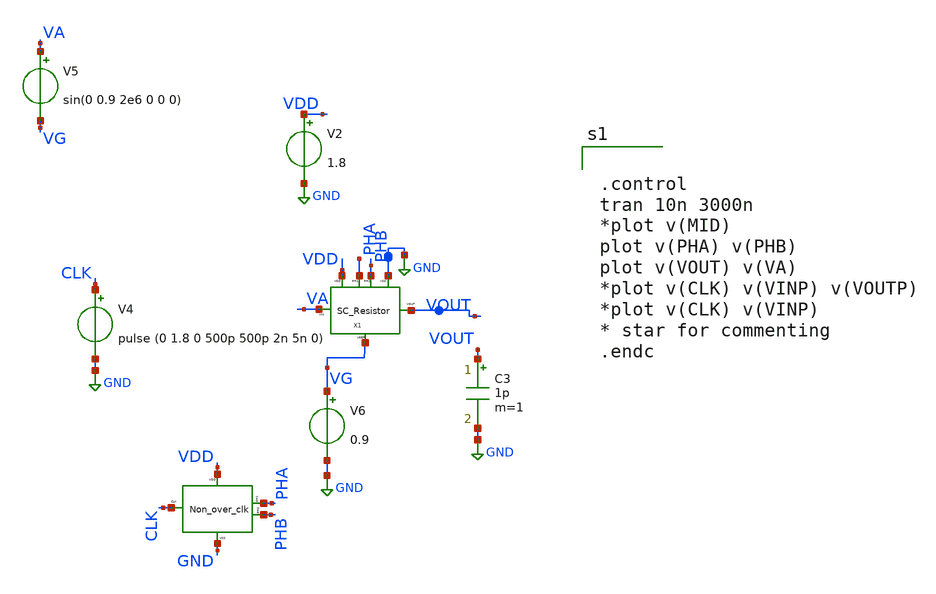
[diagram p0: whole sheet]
** sch_path: xschem/xschem_BGR_Top/Sigma_Delta/SC_Resistor/SC_Resistor_TB.sch
**.subckt SC_Resistor_TB
V2 VDD GND 1.8
V6 VG GND 0.9
X1 VG PHB VOUT VDD GND PHA VA SC_Resistor
V5 VA VG sin(0 0.9 2e6 0 0 0)
X2 PHB VDD GND PHA CLK Non_over_clk
V4 CLK GND pulse (0 1.8 0 500p 500p 2n 5n 0)
C3 VOUT GND 1p m=1
**** begin user architecture code


.control
tran 10n 3000n
*plot v(MID)
plot v(PHA) v(PHB)
plot v(VOUT) v(VA)
*plot v(CLK) v(VINP) v(VOUTP)
*plot v(CLK) v(VINP)
* star for commenting
.endc


** opencircuitdesign pdks install
.lib $::SKYWATER_MODELS/sky130.lib.spice tt


**** end user architecture code
**.ends

* expanding   symbol:  Sigma_Delta/SC_Resistor/SC_Resistor.sym # of pins=7
** sym_path: xschem/xschem_BGR_Top/Sigma_Delta/SC_Resistor/SC_Resistor.sym
** sch_path: xschem/xschem_BGR_Top/Sigma_Delta/SC_Resistor/SC_Resistor.sch
.subckt SC_Resistor VREF PH2 VOUT VDD VSS PH1 VIN
*.iopin VDD
*.iopin PH1
*.iopin VIN
*.iopin VOUT
*.iopin PH2
*.iopin VREF
*.iopin VSS
XTG3 VSS PH1 VDD VIN MID1 TG
XTG4 VSS PH2 VDD MID2 VOUT TG
XM2 MID1 PH2 VREF VSS sky130_fd_pr__nfet_01v8 L=0.15 W=20 nf=2 ad='int((nf+1)/2) * W/nf * 0.29' as='int((nf+2)/2) * W/nf * 0.29'
+ pd='2*int((nf+1)/2) * (W/nf + 0.29)' ps='2*int((nf+2)/2) * (W/nf + 0.29)' nrd='0.29 / W' nrs='0.29 / W'
+ sa=0 sb=0 sd=0 mult=1 m=1
XM1 MID2 PH1 VREF VSS sky130_fd_pr__nfet_01v8 L=0.15 W=20 nf=2 ad='int((nf+1)/2) * W/nf * 0.29' as='int((nf+2)/2) * W/nf * 0.29'
+ pd='2*int((nf+1)/2) * (W/nf + 0.29)' ps='2*int((nf+2)/2) * (W/nf + 0.29)' nrd='0.29 / W' nrs='0.29 / W'
+ sa=0 sb=0 sd=0 mult=1 m=1
XC2 MID2 MID1 sky130_fd_pr__cap_mim_m3_2 W=32 L=32 MF=1 m=1
.ends


* expanding   symbol:  Sigma_Delta/Non_over_clk/Non_over_clk.sym # of pins=5
** sym_path: xschem/xschem_BGR_Top/Sigma_Delta/Non_over_clk/Non_over_clk.sym
** sch_path: xschem/xschem_BGR_Top/Sigma_Delta/Non_over_clk/Non_over_clk.sch
.subckt Non_over_clk PH2 VDD VSS PH1 CLK
*.iopin VDD
*.iopin VSS
*.iopin CLK
*.iopin PH1
*.iopin PH2
X1 VSS VDD CLK net1 Inverter
X2 VSS VDD net9 PH1 Inverter
X3 VSS VDD net8 PH2 Inverter
X4 VSS VDD net3 net2 INV_1x64
X5 VSS VDD net5 net4 INV_1x64
XNOR1 VDD VSS net1 PH2 net3 NOR
XNOR2 VDD VSS CLK PH1 net5 NOR
X8 VSS VDD net6 net8 Inverter
X9 VSS VDD net7 net9 Inverter
X6 VSS VDD net2 net7 INV_1x64
X7 VSS VDD net4 net6 INV_1x64
.ends


* expanding   symbol:  Sigma_Delta/Transmission_Gate/TG.sym # of pins=5
** sym_path: xschem/xschem_BGR_Top/Sigma_Delta/Transmission_Gate/TG.sym
** sch_path: xschem/xschem_BGR_Top/Sigma_Delta/Transmission_Gate/TG.sch
.subckt TG VSS CLK VDD A B
*.iopin VDD
*.iopin VSS
*.iopin A
*.iopin B
*.iopin CLK
XM1 A CLK B VSS sky130_fd_pr__nfet_01v8 L=0.15 W=10 nf=1 ad='int((nf+1)/2) * W/nf * 0.29' as='int((nf+2)/2) * W/nf * 0.29'
+ pd='2*int((nf+1)/2) * (W/nf + 0.29)' ps='2*int((nf+2)/2) * (W/nf + 0.29)' nrd='0.29 / W' nrs='0.29 / W'
+ sa=0 sb=0 sd=0 mult=1 m=1
XM2 B CLKB A VDD sky130_fd_pr__pfet_01v8 L=0.15 W=20 nf=2 ad='int((nf+1)/2) * W/nf * 0.29' as='int((nf+2)/2) * W/nf * 0.29'
+ pd='2*int((nf+1)/2) * (W/nf + 0.29)' ps='2*int((nf+2)/2) * (W/nf + 0.29)' nrd='0.29 / W' nrs='0.29 / W'
+ sa=0 sb=0 sd=0 mult=1 m=1
XM3 CLKB CLK VSS VSS sky130_fd_pr__nfet_01v8 L=0.15 W=10 nf=5 ad='int((nf+1)/2) * W/nf * 0.29' as='int((nf+2)/2) * W/nf * 0.29'
+ pd='2*int((nf+1)/2) * (W/nf + 0.29)' ps='2*int((nf+2)/2) * (W/nf + 0.29)' nrd='0.29 / W' nrs='0.29 / W'
+ sa=0 sb=0 sd=0 mult=1 m=1
XM4 CLKB CLK VDD VDD sky130_fd_pr__pfet_01v8 L=0.15 W=20 nf=10 ad='int((nf+1)/2) * W/nf * 0.29' as='int((nf+2)/2) * W/nf * 0.29'
+ pd='2*int((nf+1)/2) * (W/nf + 0.29)' ps='2*int((nf+2)/2) * (W/nf + 0.29)' nrd='0.29 / W' nrs='0.29 / W'
+ sa=0 sb=0 sd=0 mult=1 m=1
.ends


* expanding   symbol:  Sigma_Delta/Inverter/Inverter.sym # of pins=4
** sym_path: xschem/xschem_BGR_Top/Sigma_Delta/Inverter/Inverter.sym
** sch_path: xschem/xschem_BGR_Top/Sigma_Delta/Inverter/Inverter.sch
.subckt Inverter VSS VDD VIN VOUT
*.ipin VIN
*.iopin VDD
*.iopin VSS
*.opin VOUT
XM1 VOUT VIN VSS VSS sky130_fd_pr__nfet_01v8 L=0.15 W=0.9 nf=1 ad='int((nf+1)/2) * W/nf * 0.29' as='int((nf+2)/2) * W/nf * 0.29'
+ pd='2*int((nf+1)/2) * (W/nf + 0.29)' ps='2*int((nf+2)/2) * (W/nf + 0.29)' nrd='0.29 / W' nrs='0.29 / W'
+ sa=0 sb=0 sd=0 mult=1 m=1
XM2 VOUT VIN VDD VDD sky130_fd_pr__pfet_01v8 L=0.15 W=0.9 nf=2 ad='int((nf+1)/2) * W/nf * 0.29' as='int((nf+2)/2) * W/nf * 0.29'
+ pd='2*int((nf+1)/2) * (W/nf + 0.29)' ps='2*int((nf+2)/2) * (W/nf + 0.29)' nrd='0.29 / W' nrs='0.29 / W'
+ sa=0 sb=0 sd=0 mult=1 m=1
.ends


* expanding   symbol:  Sigma_Delta/INV_1x64/INV_1x64.sym # of pins=4
** sym_path: xschem/xschem_BGR_Top/Sigma_Delta/INV_1x64/INV_1x64.sym
** sch_path: xschem/xschem_BGR_Top/Sigma_Delta/INV_1x64/INV_1x64.sch
.subckt INV_1x64 VSS VDD VIN VOUT
*.ipin VIN
*.iopin VDD
*.iopin VSS
*.opin VOUT
XM1 VOUT VIN net1 VSS sky130_fd_pr__nfet_01v8 L=0.15 W=0.425 nf=1 ad='int((nf+1)/2) * W/nf * 0.29' as='int((nf+2)/2) * W/nf * 0.29'
+ pd='2*int((nf+1)/2) * (W/nf + 0.29)' ps='2*int((nf+2)/2) * (W/nf + 0.29)' nrd='0.29 / W' nrs='0.29 / W'
+ sa=0 sb=0 sd=0 mult=1 m=1
XM2 VOUT VIN net2 VDD sky130_fd_pr__pfet_01v8 L=0.15 W=0.425 nf=1 ad='int((nf+1)/2) * W/nf * 0.29' as='int((nf+2)/2) * W/nf * 0.29'
+ pd='2*int((nf+1)/2) * (W/nf + 0.29)' ps='2*int((nf+2)/2) * (W/nf + 0.29)' nrd='0.29 / W' nrs='0.29 / W'
+ sa=0 sb=0 sd=0 mult=1 m=1
XM3 net2 VIN net3 VDD sky130_fd_pr__pfet_01v8 L=0.15 W=0.425 nf=1 ad='int((nf+1)/2) * W/nf * 0.29' as='int((nf+2)/2) * W/nf * 0.29'
+ pd='2*int((nf+1)/2) * (W/nf + 0.29)' ps='2*int((nf+2)/2) * (W/nf + 0.29)' nrd='0.29 / W' nrs='0.29 / W'
+ sa=0 sb=0 sd=0 mult=1 m=1
XM4 net3 VIN net4 VDD sky130_fd_pr__pfet_01v8 L=0.15 W=0.425 nf=1 ad='int((nf+1)/2) * W/nf * 0.29' as='int((nf+2)/2) * W/nf * 0.29'
+ pd='2*int((nf+1)/2) * (W/nf + 0.29)' ps='2*int((nf+2)/2) * (W/nf + 0.29)' nrd='0.29 / W' nrs='0.29 / W'
+ sa=0 sb=0 sd=0 mult=1 m=1
XM5 net4 VIN net8 VDD sky130_fd_pr__pfet_01v8 L=0.15 W=0.425 nf=1 ad='int((nf+1)/2) * W/nf * 0.29' as='int((nf+2)/2) * W/nf * 0.29'
+ pd='2*int((nf+1)/2) * (W/nf + 0.29)' ps='2*int((nf+2)/2) * (W/nf + 0.29)' nrd='0.29 / W' nrs='0.29 / W'
+ sa=0 sb=0 sd=0 mult=1 m=1
XM6 net1 VIN net5 VSS sky130_fd_pr__nfet_01v8 L=0.15 W=0.425 nf=1 ad='int((nf+1)/2) * W/nf * 0.29' as='int((nf+2)/2) * W/nf * 0.29'
+ pd='2*int((nf+1)/2) * (W/nf + 0.29)' ps='2*int((nf+2)/2) * (W/nf + 0.29)' nrd='0.29 / W' nrs='0.29 / W'
+ sa=0 sb=0 sd=0 mult=1 m=1
XM7 net5 VIN net6 VSS sky130_fd_pr__nfet_01v8 L=0.15 W=0.425 nf=1 ad='int((nf+1)/2) * W/nf * 0.29' as='int((nf+2)/2) * W/nf * 0.29'
+ pd='2*int((nf+1)/2) * (W/nf + 0.29)' ps='2*int((nf+2)/2) * (W/nf + 0.29)' nrd='0.29 / W' nrs='0.29 / W'
+ sa=0 sb=0 sd=0 mult=1 m=1
XM8 net6 VIN net7 VSS sky130_fd_pr__nfet_01v8 L=0.15 W=0.425 nf=1 ad='int((nf+1)/2) * W/nf * 0.29' as='int((nf+2)/2) * W/nf * 0.29'
+ pd='2*int((nf+1)/2) * (W/nf + 0.29)' ps='2*int((nf+2)/2) * (W/nf + 0.29)' nrd='0.29 / W' nrs='0.29 / W'
+ sa=0 sb=0 sd=0 mult=1 m=1
XM9 net7 VIN VSS VSS sky130_fd_pr__nfet_01v8 L=0.15 W=0.425 nf=1 ad='int((nf+1)/2) * W/nf * 0.29' as='int((nf+2)/2) * W/nf * 0.29'
+ pd='2*int((nf+1)/2) * (W/nf + 0.29)' ps='2*int((nf+2)/2) * (W/nf + 0.29)' nrd='0.29 / W' nrs='0.29 / W'
+ sa=0 sb=0 sd=0 mult=1 m=1
XM10 net8 VIN VDD VDD sky130_fd_pr__pfet_01v8 L=0.15 W=0.425 nf=1 ad='int((nf+1)/2) * W/nf * 0.29' as='int((nf+2)/2) * W/nf * 0.29'
+ pd='2*int((nf+1)/2) * (W/nf + 0.29)' ps='2*int((nf+2)/2) * (W/nf + 0.29)' nrd='0.29 / W' nrs='0.29 / W'
+ sa=0 sb=0 sd=0 mult=1 m=1
.ends


* expanding   symbol:  Sigma_Delta/Nor/NOR.sym # of pins=5
** sym_path: xschem/xschem_BGR_Top/Sigma_Delta/Nor/NOR.sym
** sch_path: xschem/xschem_BGR_Top/Sigma_Delta/Nor/NOR.sch
.subckt NOR VDD VSS A B OUT
*.iopin VDD
*.iopin VSS
*.iopin A
*.iopin B
*.iopin OUT
XM2 OUT A VSS VSS sky130_fd_pr__nfet_01v8 L=0.15 W=0.5 nf=1 ad='int((nf+1)/2) * W/nf * 0.29' as='int((nf+2)/2) * W/nf * 0.29'
+ pd='2*int((nf+1)/2) * (W/nf + 0.29)' ps='2*int((nf+2)/2) * (W/nf + 0.29)' nrd='0.29 / W' nrs='0.29 / W'
+ sa=0 sb=0 sd=0 mult=1 m=1
XM3 net1 A VDD VDD sky130_fd_pr__pfet_01v8 L=0.15 W=0.5 nf=1 ad='int((nf+1)/2) * W/nf * 0.29' as='int((nf+2)/2) * W/nf * 0.29'
+ pd='2*int((nf+1)/2) * (W/nf + 0.29)' ps='2*int((nf+2)/2) * (W/nf + 0.29)' nrd='0.29 / W' nrs='0.29 / W'
+ sa=0 sb=0 sd=0 mult=1 m=1
XM1 OUT B net1 VDD sky130_fd_pr__pfet_01v8 L=0.15 W=0.5 nf=1 ad='int((nf+1)/2) * W/nf * 0.29' as='int((nf+2)/2) * W/nf * 0.29'
+ pd='2*int((nf+1)/2) * (W/nf + 0.29)' ps='2*int((nf+2)/2) * (W/nf + 0.29)' nrd='0.29 / W' nrs='0.29 / W'
+ sa=0 sb=0 sd=0 mult=1 m=1
XM4 OUT B VSS VSS sky130_fd_pr__nfet_01v8 L=0.15 W=0.5 nf=1 ad='int((nf+1)/2) * W/nf * 0.29' as='int((nf+2)/2) * W/nf * 0.29'
+ pd='2*int((nf+1)/2) * (W/nf + 0.29)' ps='2*int((nf+2)/2) * (W/nf + 0.29)' nrd='0.29 / W' nrs='0.29 / W'
+ sa=0 sb=0 sd=0 mult=1 m=1
.ends

.GLOBAL GND
.end
